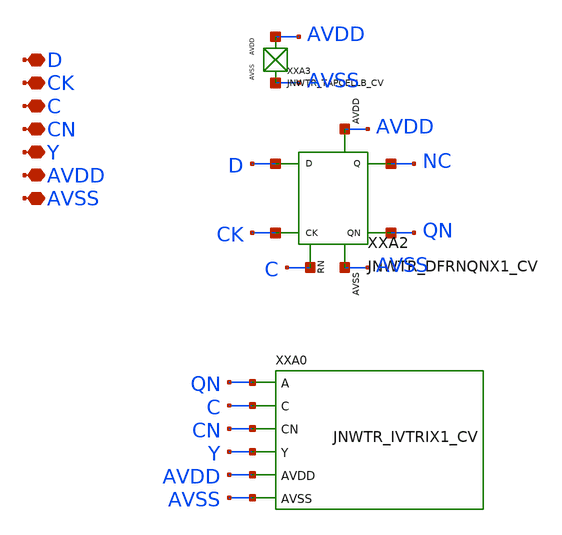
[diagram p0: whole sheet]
** sch_path: design/JNW_TR_SKY130A/JNWTR_DFTRIX1_CV.sch
**.subckt JNWTR_DFTRIX1_CV D CK C CN Y AVDD AVSS
*.iopin D
*.iopin CK
*.iopin C
*.iopin CN
*.iopin Y
*.iopin AVDD
*.iopin AVSS
XXA3 AVDD AVSS JNWTR_TAPCELLB_CV xoffset=0 yoffset=0 angle=0
XXA2 D CK C NC QN AVDD AVSS JNWTR_DFRNQNX1_CV xoffset=0 yoffset=0 angle=0
XXA0 QN C CN Y AVDD AVSS JNWTR_IVTRIX1_CV xoffset=0 yoffset=0 angle=0
**.ends
.end
